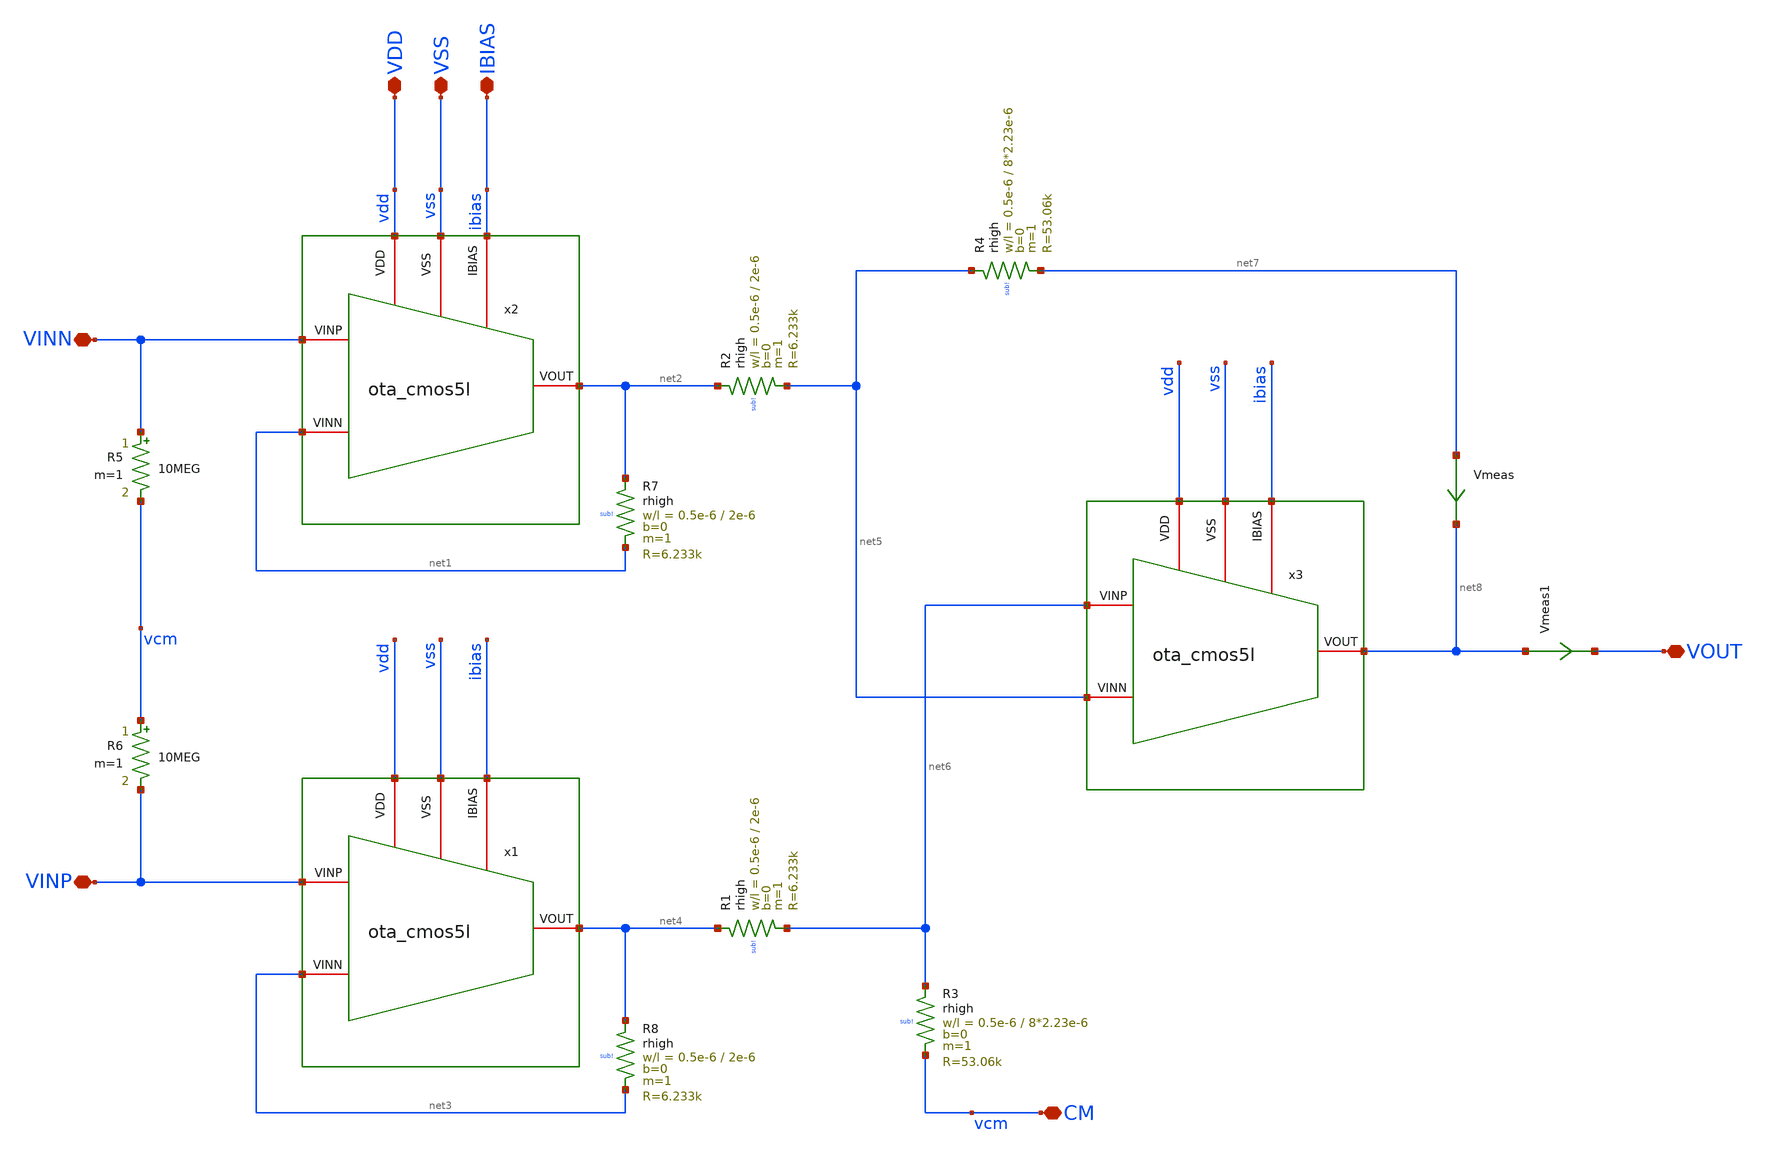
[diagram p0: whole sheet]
** sch_path: xschem/instramp_cmos5l/instramp_cmos5l.sch
**.subckt instramp_cmos5l VDD IBIAS VSS CM VOUT VINN VINP
*.iopin VDD
*.iopin IBIAS
*.iopin VSS
*.iopin CM
*.iopin VOUT
*.iopin VINN
*.iopin VINP
x1 vss ibias vdd net3 VINP net4 ota_cmos5l
x2 vss ibias vdd net1 VINN net2 ota_cmos5l
x3 vss ibias vdd net5 net6 net8 ota_cmos5l
XR1 net4 net6 sub! rhigh w=0.5e-6 l=2e-6 m=1 b=0 mm_ok=1
XR2 net2 net5 sub! rhigh w=0.5e-6 l=2e-6 m=1 b=0 mm_ok=1
XR3 net6 CM sub! rhigh w=0.5e-6 l=8*2.23e-6 m=1 b=0 mm_ok=1
XR4 net5 net7 sub! rhigh w=0.5e-6 l=8*2.23e-6 m=1 b=0 mm_ok=1
Vmeas net7 net8 0
.save i(vmeas)
Vmeas1 net8 VOUT 0
.save i(vmeas1)
R5 VINN vcm 10MEG m=1
R6 vcm VINP 10MEG m=1
XR7 net2 net1 sub! rhigh w=0.5e-6 l=2e-6 m=1 b=0 mm_ok=1
XR8 net4 net3 sub! rhigh w=0.5e-6 l=2e-6 m=1 b=0 mm_ok=1
**.ends

* expanding   symbol:  /foss/designs/sg13cmos5l_spma_ip__instramp/xschem/ota_cmos5l/ota_cmos5l.sym #
*+ of pins=6
** sym_path: xschem/output_buffer/ota_cmos5l.sym
** sch_path: xschem/output_buffer/ota_cmos5l.sch
.subckt ota_cmos5l VSS IBIAS VDD VINN VINP VOUT
*.iopin IBIAS
*.iopin VDD
*.iopin VSS
*.iopin VOUT
*.iopin VINP
*.iopin VINN
XM6 IBIAS IBIAS VDD VDD sg13_lv_pmos w={wbias} l={lbias} ng=1 m={m6} mm_ok=1
XM7 net1 IBIAS VDD VDD sg13_lv_pmos w={wbias} l={lbias} ng=1 m={m7} mm_ok=1
XM8 VOUT IBIAS VDD VDD sg13_lv_pmos w={wbias} l={lbias} ng=1 m={m8} mm_ok=1
XM1 net2 VINN net1 VDD sg13_lv_pmos w={winpair} l={linpair} ng=1 m=1 mm_ok=1
XM2 net3 VINP net1 VDD sg13_lv_pmos w={winpair} l={linpair} ng=1 m=1 mm_ok=1
XM3 net2 net2 VSS VSS sg13_lv_nmos w={wload} l={lload} ng=1 m=1 mm_ok=1
XM4 net3 net2 VSS VSS sg13_lv_nmos w={wload} l={lload} ng=1 m=1 mm_ok=1
XM5 VOUT net3 VSS VSS sg13_lv_nmos w={wcs} l={lcs} ng=1 m=1 mm_ok=1
XR1 net3 net4 VSS rhigh w=0.5e-6 l=1.95e-6 m=1 b=0 mm_ok=1
.save v(vinp)
.save v(vinn)
.save v(vout)
XC2 VOUT net4 cap_cmomi w=15e-6 l=15e-6 mmin=1 mmax=4 feed=double subblock=0 m=5 mm_ok=1
**** begin user architecture code


.param temp=27
.param lbias=0.15u wbias=0.15u
.param m6=1 m7=4 m8=8
.param linpair=3u winpair=20u
.param lload=5u wload=10u
.param lcs=3u wcs=20u
.param Cc=2p



**** end user architecture code
XC1 VOUT net4 cap_cmomi w=15e-6 l=15e-6 mmin=1 mmax=4 feed=double subblock=0 m=4 mm_ok=1
.ends

.end
